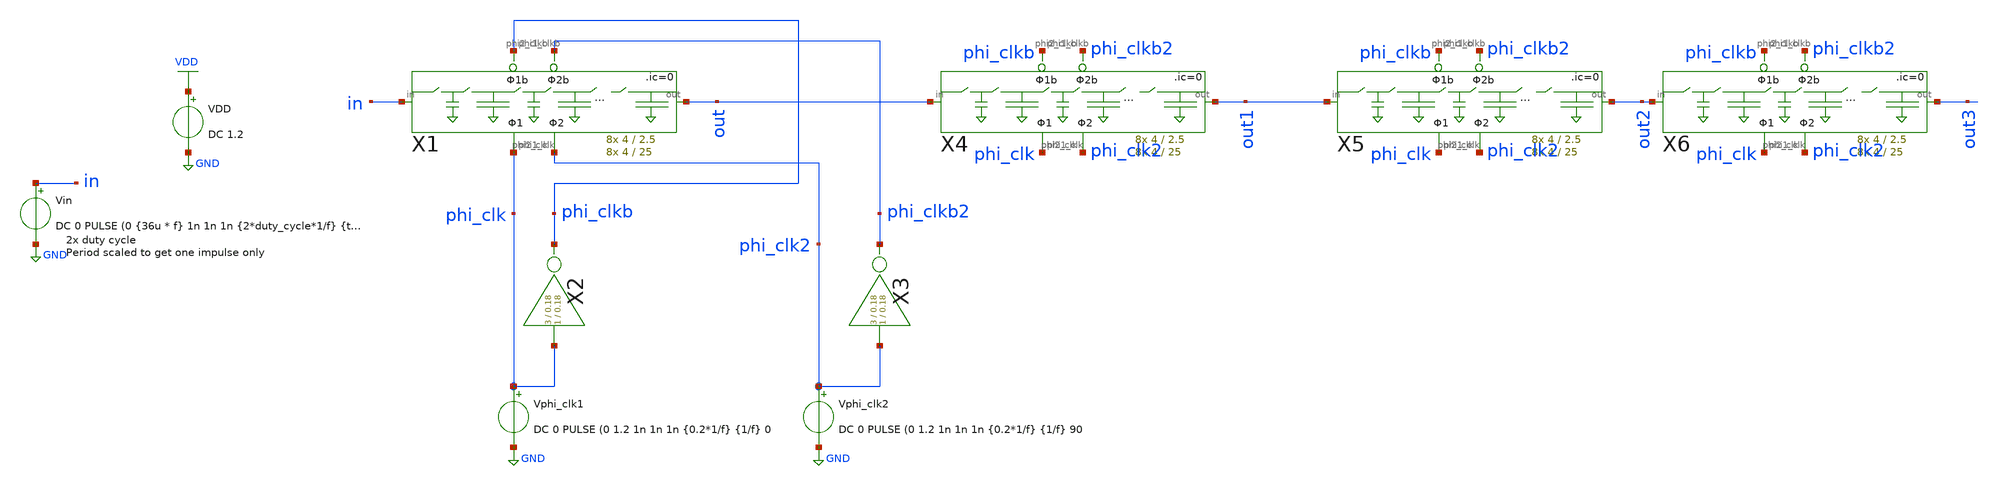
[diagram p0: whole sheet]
** sch_path: xschem/Switched_Caps/testing4.sch
**.subckt testing4
Vin in GND DC 0 PULSE (0 {36u * f} 1n 1n 1n {2*duty_cycle*1/f} {tend}
VDD VDD GND DC 1.2
X2 phi_clk phi_clkb inv Wpmos=3 Lpmos=0.18 Wnmos=1 Lnmos=0.18
Vphi_clk1 phi_clk GND DC 0 PULSE (0 1.2 1n 1n 1n {0.2*1/f} {1/f} 0
X1 in out phi_clk phi_clkb phi_clk2 phi_clkb2 16switchcaps_2phi Wcap1=4 Lcap1=2.5 Wcap2=4 Lcap2=25
Vphi_clk2 phi_clk2 GND DC 0 PULSE (0 1.2 1n 1n 1n {0.2*1/f} {1/f} 90
X3 phi_clk2 phi_clkb2 inv Wpmos=3 Lpmos=0.18 Wnmos=1 Lnmos=0.18
X4 out out1 phi_clk phi_clkb phi_clk2 phi_clkb2 16switchcaps_2phi Wcap1=4 Lcap1=2.5 Wcap2=4 Lcap2=25
X5 out1 out2 phi_clk phi_clkb phi_clk2 phi_clkb2 16switchcaps_2phi Wcap1=4 Lcap1=2.5 Wcap2=4
+ Lcap2=25
X6 out2 out3 phi_clk phi_clkb phi_clk2 phi_clkb2 16switchcaps_2phi Wcap1=4 Lcap1=2.5 Wcap2=4
+ Lcap2=25
**** begin user architecture code


.lib /home/sky/sky130A/libs.tech/ngspice/sky130.lib.spice tt
.options abstol=1e-14 reltol=1e-4
.param f=2560k
.param duty_cycle=0.5
.param tau={(48^2)*1/f}
.param tend={4*tau}

*start all caps with 0 charge
.ic v(x1.x1.c1)=0 v(x1.c2)=0 v(x1.x2.c1)=0 v(x1.c4)=0   v(x1.x3.c1)=0 v(x1.c6)=0 v(x1.x4.c1)=0
+ v(x1.c8)=0   v(x1.x5.c1)=0 v(x1.c10)=0 v(x1.x6.c1)=0 v(x1.c12)=0   v(x1.x7.c1)=0 v(x1.c14)=0 v(x1.x8.c1)=0
+ v(out)=0  v(x4.x1.c1)=0 v(x4.c2)=0 v(x4.x2.c1)=0 v(x4.c4)=0   v(x4.x3.c1)=0 v(x4.c6)=0 v(x4.x4.c1)=0
+ v(x4.c8)=0   v(x4.x5.c1)=0 v(x4.c10)=0 v(x4.x6.c1)=0 v(x4.c12)=0   v(x4.x7.c1)=0 v(x4.c14)=0 v(x4.x8.c1)=0
+ v(out1)=0  v(x5.x1.c1)=0 v(x5.c2)=0 v(x5.x2.c1)=0 v(x5.c4)=0   v(x5.x3.c1)=0 v(x5.c6)=0 v(x5.x4.c1)=0
+ v(x5.c8)=0   v(x5.x5.c1)=0 v(x5.c10)=0 v(x5.x6.c1)=0 v(x5.c12)=0   v(x5.x7.c1)=0 v(x5.c14)=0 v(x5.x8.c1)=0
+ v(out2)=0  v(x6.x1.c1)=0 v(x6.c2)=0 v(x6.x2.c1)=0 v(x6.c4)=0   v(x6.x3.c1)=0 v(x6.c6)=0 v(x6.x4.c1)=0
+ v(x6.c8)=0   v(x6.x5.c1)=0 v(x6.c10)=0 v(x6.x6.c1)=0 v(x6.c12)=0   v(x6.x7.c1)=0 v(x6.c14)=0 v(x6.x8.c1)=0
+ v(out3)=0


*.ac DEC 100 10 20k *doesn't seem to work, get 0s out
.tran {1/f} {tend}
.save all


**** end user architecture code
**.ends
.GLOBAL GND
.GLOBAL VDD
.end
